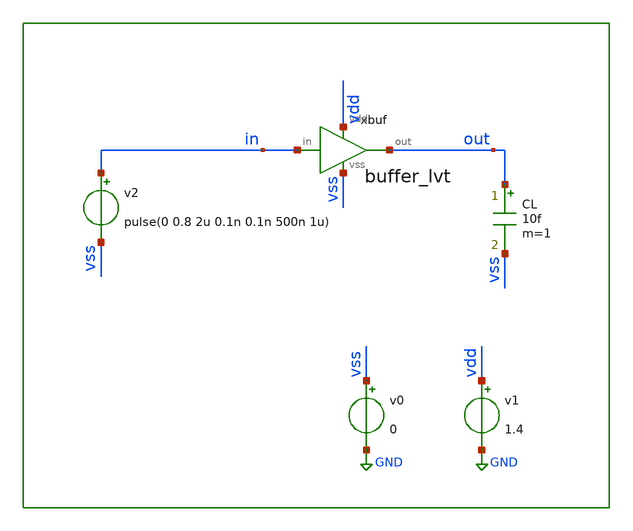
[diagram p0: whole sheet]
** sch_path: xschem/tb/sar_10b/tr_buffer.sch
**.subckt tr_buffer
v0 vss GND 0
v1 vdd GND 1.4
v2 in vss pulse(0 0.8 2u 0.1n 0.1n 500n 1u)
CL out vss 10f m=1
xbuf vdd in out vss buffer_lvt
**** begin user architecture code
.options method trap
.option vntol 1e-6

.control
.param MC_SWITCH=0
tran 1e-9 10e-6
run
.endc


* FET CORNERS
.include $::SKYWATER_MODELS/corners/tt.spice
*.include $::SKYWATER_MODELS/corners/ff.spice
*.include $::SKYWATER_MODELS/corners/ss.spice
*.include $::SKYWATER_MODELS/corners/sf.spice
*.include $::SKYWATER_MODELS/corners/fs.spice

* TT + R + C
*.include $::SKYWATER_MODELS/corners/tt_rmax_cmax.spice
*.include $::SKYWATER_MODELS/corners/tt_rmin_cmin.spice
*.include $::SKYWATER_MODELS/corners/tt_rmax_cmin.spice
*.include $::SKYWATER_MODELS/corners/tt_rmin_cmax.spice

* FF + R + C
*.include $::SKYWATER_MODELS/corners/ff_rmax_cmax.spice
*.include $::SKYWATER_MODELS/corners/ff_rmin_cmin.spice
*.include $::SKYWATER_MODELS/corners/ff_rmax_cmin.spice
*.include $::SKYWATER_MODELS/corners/ff_rmin_cmax.spice


* SS + R + C
*.include $::SKYWATER_MODELS/corners/ss_rmax_cmax.spice
*.include $::SKYWATER_MODELS/corners/ss_rmin_cmin.spice
*.include $::SKYWATER_MODELS/corners/ss_rmax_cmin.spice
*.include $::SKYWATER_MODELS/corners/ss_rmin_cmax.spice

* SF + R + C
*.include $::SKYWATER_MODELS/corners/sf_rmax_cmax.spice
*.include $::SKYWATER_MODELS/corners/sf_rmin_cmin.spice
*.include $::SKYWATER_MODELS/corners/sf_rmax_cmin.spice
*.include $::SKYWATER_MODELS/corners/sf_rmin_cmax.spice

* FS + R + C
*.include $::SKYWATER_MODELS/corners/fs_rmax_cmax.spice
*.include $::SKYWATER_MODELS/corners/fs_rmin_cmin.spice
*.include $::SKYWATER_MODELS/corners/fs_rmax_cmin.spice
*.include $::SKYWATER_MODELS/corners/fs_rmin_cmax.spice

**** end user architecture code
**.ends

* expanding   symbol:  logic/buffer_lvt.sym # of pins=4
** sym_path: xschem/logic/buffer_lvt.sym
** sch_path: xschem/logic/buffer_lvt.sch
.subckt buffer_lvt vdd in out vss
*.iopin vdd
*.iopin vss
*.ipin in
*.opin out
XM1 net1 in vss vss sky130_fd_pr__nfet_01v8_lvt L=0.4 W=1 nf=1 ad='int((nf+1)/2) * W/nf * 0.29' as='int((nf+2)/2) * W/nf * 0.29'
+ pd='2*int((nf+1)/2) * (W/nf + 0.29)' ps='2*int((nf+2)/2) * (W/nf + 0.29)' nrd='0.29 / W' nrs='0.29 / W'
+ sa=0 sb=0 sd=0 mult=1 m=1
XM2 net1 in vdd vdd sky130_fd_pr__pfet_01v8_lvt L=0.4 W=1 nf=1 ad='int((nf+1)/2) * W/nf * 0.29' as='int((nf+2)/2) * W/nf * 0.29'
+ pd='2*int((nf+1)/2) * (W/nf + 0.29)' ps='2*int((nf+2)/2) * (W/nf + 0.29)' nrd='0.29 / W' nrs='0.29 / W'
+ sa=0 sb=0 sd=0 mult=1 m=1
XM3 out net1 vss vss sky130_fd_pr__nfet_01v8_lvt L=0.4 W=1 nf=1 ad='int((nf+1)/2) * W/nf * 0.29' as='int((nf+2)/2) * W/nf * 0.29'
+ pd='2*int((nf+1)/2) * (W/nf + 0.29)' ps='2*int((nf+2)/2) * (W/nf + 0.29)' nrd='0.29 / W' nrs='0.29 / W'
+ sa=0 sb=0 sd=0 mult=1 m=1
XM4 out net1 vdd vdd sky130_fd_pr__pfet_01v8_lvt L=0.4 W=1 nf=1 ad='int((nf+1)/2) * W/nf * 0.29' as='int((nf+2)/2) * W/nf * 0.29'
+ pd='2*int((nf+1)/2) * (W/nf + 0.29)' ps='2*int((nf+2)/2) * (W/nf + 0.29)' nrd='0.29 / W' nrs='0.29 / W'
+ sa=0 sb=0 sd=0 mult=1 m=1
.ends

.GLOBAL GND
.end
